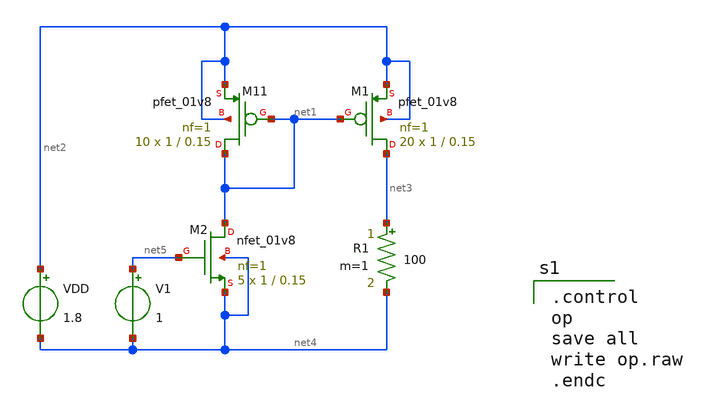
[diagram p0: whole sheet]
** sch_path: current_mirror.sch
**.subckt current_mirror
XM11 net1 net1 net2 net2 sky130_fd_pr__pfet_01v8 L=0.15 W=1 nf=1 ad='int((nf+1)/2) * W/nf * 0.29' as='int((nf+2)/2) * W/nf * 0.29'
+ pd='2*int((nf+1)/2) * (W/nf + 0.29)' ps='2*int((nf+2)/2) * (W/nf + 0.29)' nrd='0.29 / W' nrs='0.29 / W'
+ sa=0 sb=0 sd=0 mult=10 m=10
XM1 net3 net1 net2 net2 sky130_fd_pr__pfet_01v8 L=0.15 W=1 nf=1 ad='int((nf+1)/2) * W/nf * 0.29' as='int((nf+2)/2) * W/nf * 0.29'
+ pd='2*int((nf+1)/2) * (W/nf + 0.29)' ps='2*int((nf+2)/2) * (W/nf + 0.29)' nrd='0.29 / W' nrs='0.29 / W'
+ sa=0 sb=0 sd=0 mult=20 m=20
R1 net3 net4 100 m=1
XM2 net1 net5 net4 net4 sky130_fd_pr__nfet_01v8 L=0.15 W=1 nf=1 ad='int((1 + 1)/2) * 1 / 1 * 0.29' as='int((1 + 2)/2) * 1 / 1 * 0.29'
+ pd='2*int((1 + 1)/2) * (1 / 1 + 0.29)' ps='2*int((1 + 2)/2) * (1 / 1 + 0.29)' nrd='0.29 / 1 ' nrs='0.29 / 1 '
+ sa=0 sb=0 sd=0 mult=5 m=5
V1 net5 net4 1
VDD net2 net4 1.8
**** begin user architecture code

** opencircuitdesign pdks install
.lib $::SKYWATER_MODELS/sky130.lib.spice tt



.control
op
save all
write op.raw
.endc

**** end user architecture code
**.ends
.end
